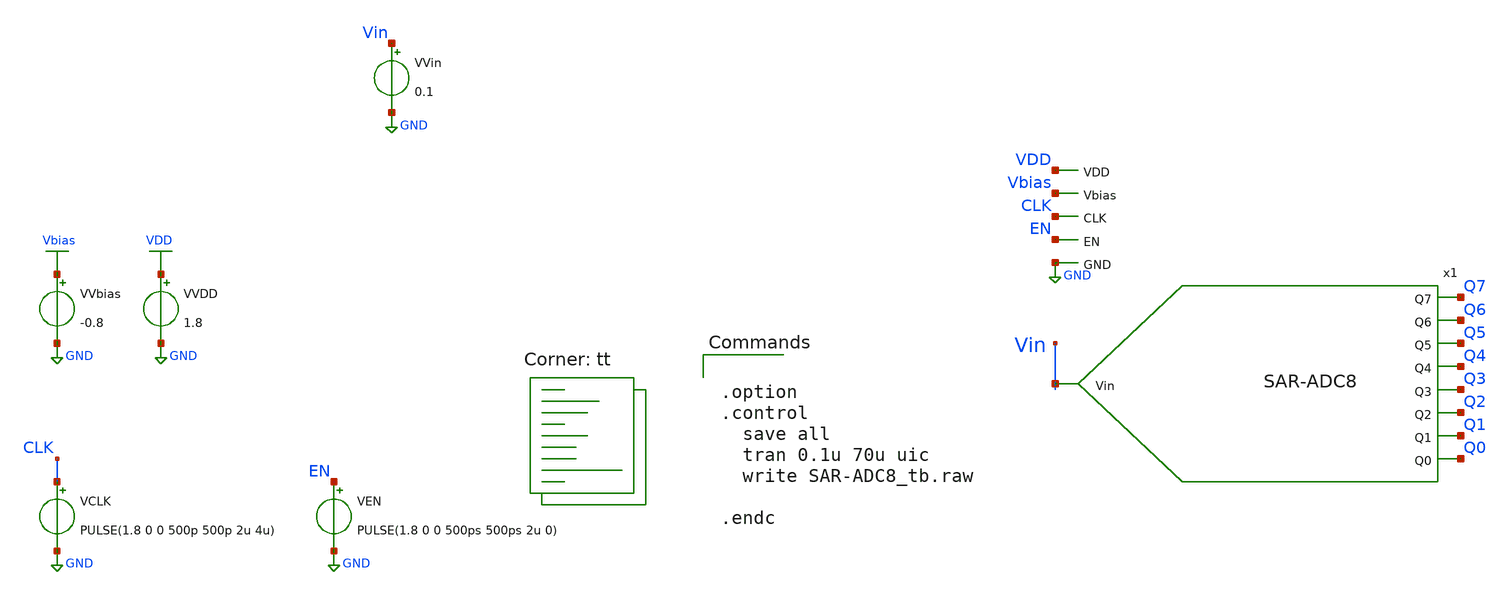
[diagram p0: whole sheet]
** sch_path: xschem/schematic/SAR-ADC8_tb.sch
**.subckt SAR-ADC8_tb
x1 VDD Vin Q0 Vbias EN Q1 CLK Q2 Q3 Q4 Q5 Q6 Q7 GND SAR-ADC8
VCLK CLK GND PULSE(1.8 0 0 500p 500p 2u 4u)
VVDD VDD GND 1.8
VEN EN GND PULSE(1.8 0 0 500ps 500ps 2u 0)
VVbias Vbias GND -0.8
VVin Vin GND 0.1
**** begin user architecture code


.option
.control
  save all
  tran 0.1u 70u uic
  write SAR-ADC8_tb.raw

.endc


.lib $::SKYWATER_MODELS/sky130.lib.spice tt
**** end user architecture code
**.ends
.GLOBAL GND
.GLOBAL VDD
.GLOBAL Vbias
.end
